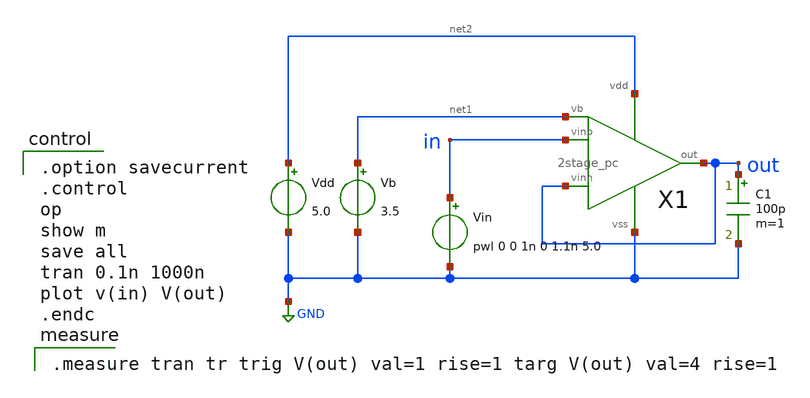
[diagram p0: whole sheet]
** sch_path: OpenSUSI-TR10/opamp/2stage_pc_tran.sch
**.subckt 2stage_pc_tran
Vdd net2 GND 5.0
Vb net1 GND 3.5
C1 out GND 100p m=1
Vin in GND pwl 0 0 1n 0 1.1n 5.0
X1 in out net1 out net2 GND 2stage_pc
**** begin user architecture code

.option savecurrent
.control
op
show m
save all
tran 0.1n 1000n
plot v(in) V(out)
.endc


.measure tran tr trig V(out) val=1 rise=1 targ V(out) val=4 rise=1

 .include $::LIB/ip62_models
**** end user architecture code
**.ends

* expanding   symbol:  2stage_pc.sym # of pins=6
** sym_path: 2stage_pc.sym
** sch_path: 2stage_pc.sch
.subckt 2stage_pc vinp vinn vb out vdd vss
*.ipin vinp
*.ipin vinn
*.ipin vb
*.opin out
*.iopin vdd
*.iopin vss
X1 vinp vinn net2 vdd vss vb diff
X2 net2 vb out vdd vss cs
XM6 net1 vb vdd vdd PMOS w=30u l=1u as=0 ad=0 ps=0 pd=0 nrd=0 nrs=0 m=1
XM1 net1 net1 net4 vss NMOS w=10u l=1u as=0 ad=0 ps=0 pd=0 nrd=0 nrs=0 m=1
XM7 net4 net4 vss vss NMOS w=10u l=1u as=0 ad=0 ps=0 pd=0 nrd=0 nrs=0 m=1
XM2 net3 net1 net2 vss NMOS w=20u l=1u as=0 ad=0 ps=0 pd=0 nrd=0 nrs=0 m=1
XC1 net3 out vss F_CSIO c=8.856p x=120u y=120u m=1
.ends


* expanding   symbol:  diff.sym # of pins=6
** sym_path: diff.sym
** sch_path: diff.sch
.subckt diff vinp vinn out vdd vss vb
*.ipin vinn
*.ipin vinp
*.ipin vb
*.opin out
*.iopin vdd
*.iopin vss
M5 net2 vb vdd vdd pmos L=2u W=40u m=1
M1 net1 vinn net2 net2 pmos L=2u W=200u m=1
M2 out vinp net2 net2 pmos L=2u W=200u m=1
M3 net1 net1 vss vss nmos L=2u W=10u m=1
M4 out net1 vss vss nmos L=2u W=10u m=1
.ends


* expanding   symbol:  cs.sym # of pins=5
** sym_path: cs.sym
** sch_path: cs.sch
.subckt cs vin vb out vdd vss
*.ipin vb
*.ipin vin
*.opin out
*.iopin vss
*.iopin vdd
XM6 out vb vdd vdd PMOS w=270u l=1u as=0 ad=0 ps=0 pd=0 nrd=0 nrs=0 m=1
XM7 out vin vss vss NMOS w=90u l=1u as=0 ad=0 ps=0 pd=0 nrd=0 nrs=0 m=1
.ends

.GLOBAL GND
.end
